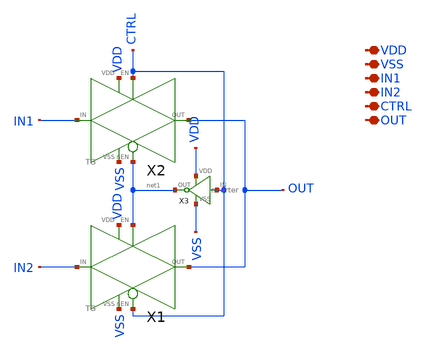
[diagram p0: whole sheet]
** sch_path: xschem/MISC/MUX/MUX.sch
**.subckt MUX VDD VSS IN1 IN2 CTRL OUT
*.iopin VDD
*.iopin VSS
*.iopin IN1
*.iopin IN2
*.iopin CTRL
*.iopin OUT
X1 CTRL IN2 OUT net1 VDD VSS TG
X2 net1 IN1 OUT CTRL VDD VSS TG
X3 CTRL VSS net1 VDD inverter
**.ends
.end
